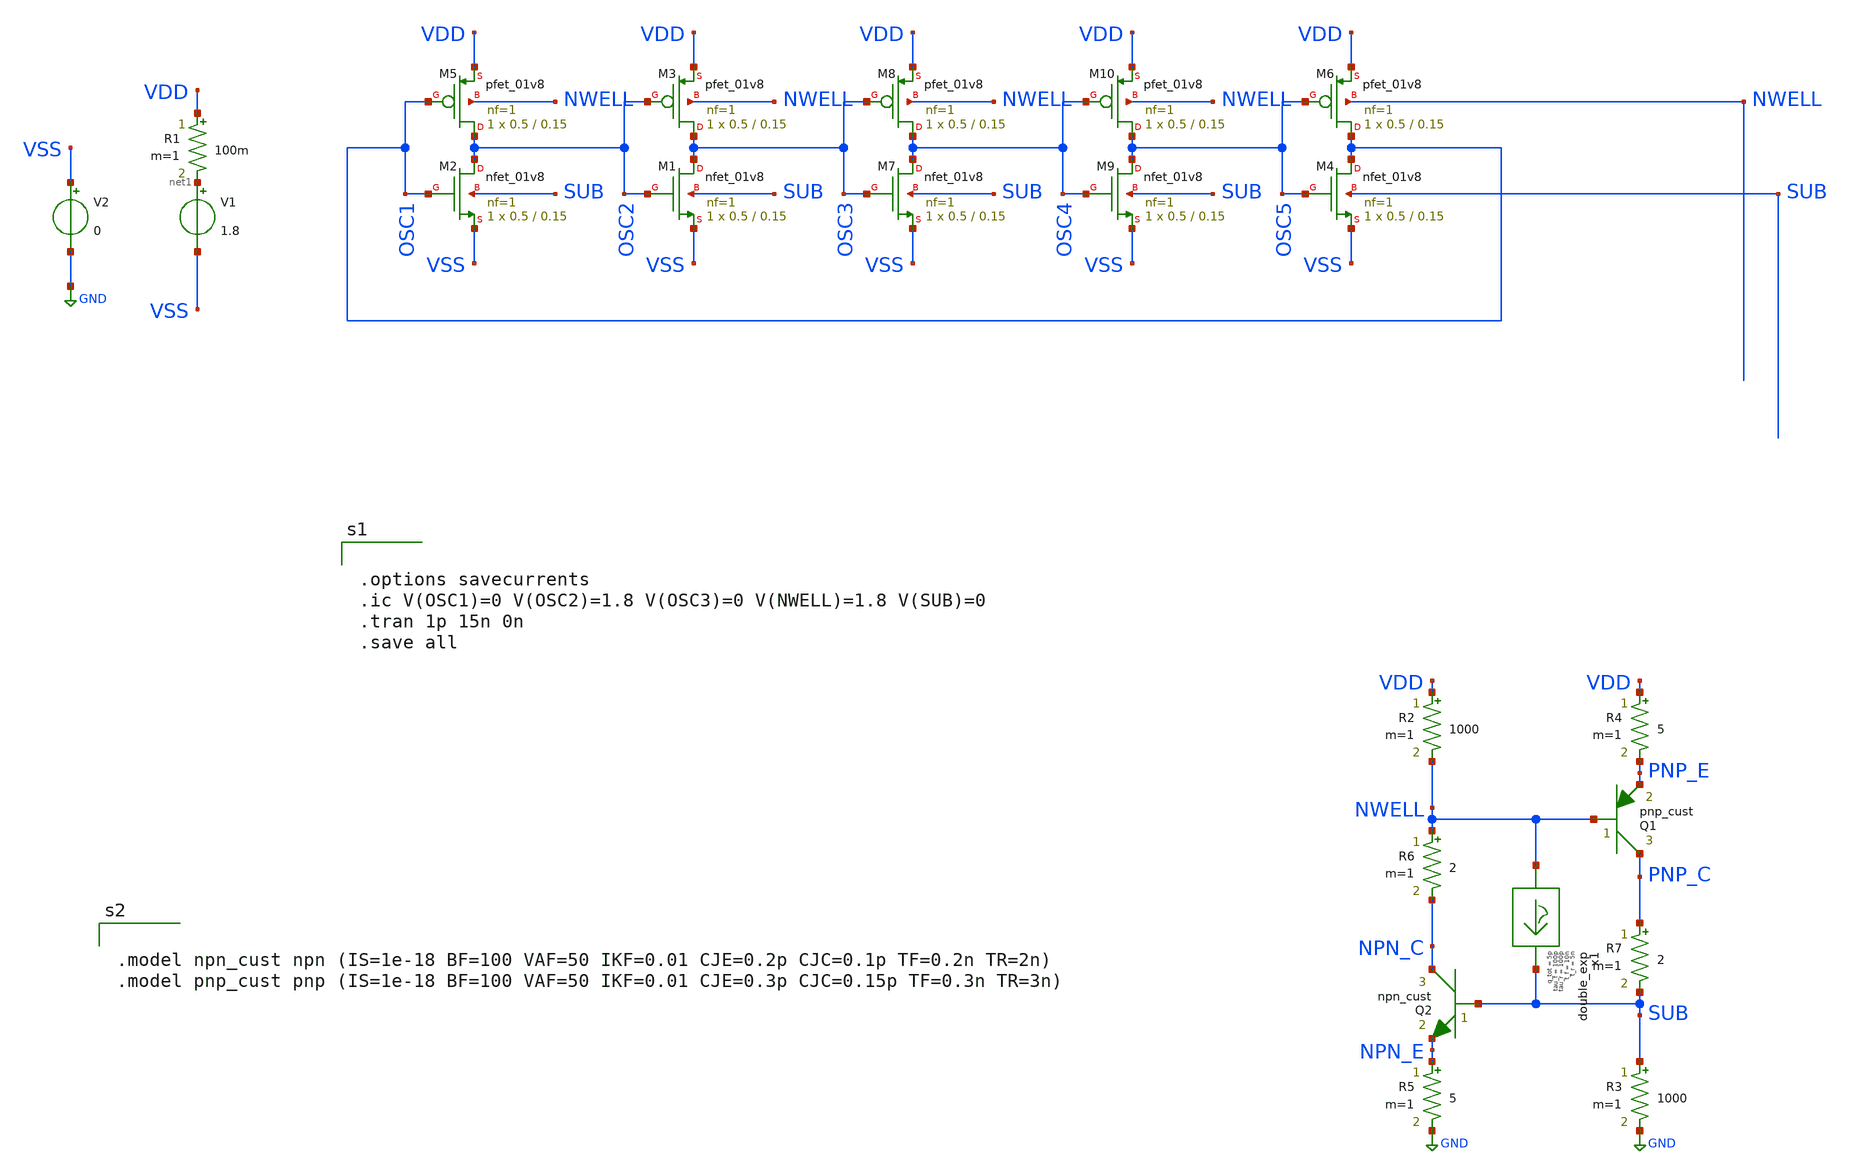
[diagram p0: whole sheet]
** sch_path: latchup/ring_osc_test_intermed.sch
**.subckt ring_osc_test_intermed
XM2 OSC2 OSC1 VSS SUB sky130_fd_pr__nfet_01v8 L=0.15 W=0.5 nf=1 ad='int((nf+1)/2) * W/nf * 0.29' as='int((nf+2)/2) * W/nf * 0.29'
+ pd='2*int((nf+1)/2) * (W/nf + 0.29)' ps='2*int((nf+2)/2) * (W/nf + 0.29)' nrd='0.29 / W' nrs='0.29 / W'
+ sa=0 sb=0 sd=0 mult=1 m=1
XM5 OSC2 OSC1 VDD NWELL sky130_fd_pr__pfet_01v8 L=0.15 W=0.5 nf=1 ad='int((nf+1)/2) * W/nf * 0.29' as='int((nf+2)/2) * W/nf * 0.29'
+ pd='2*int((nf+1)/2) * (W/nf + 0.29)' ps='2*int((nf+2)/2) * (W/nf + 0.29)' nrd='0.29 / W' nrs='0.29 / W'
+ sa=0 sb=0 sd=0 mult=1 m=1
XM1 OSC3 OSC2 VSS SUB sky130_fd_pr__nfet_01v8 L=0.15 W=0.5 nf=1 ad='int((nf+1)/2) * W/nf * 0.29' as='int((nf+2)/2) * W/nf * 0.29'
+ pd='2*int((nf+1)/2) * (W/nf + 0.29)' ps='2*int((nf+2)/2) * (W/nf + 0.29)' nrd='0.29 / W' nrs='0.29 / W'
+ sa=0 sb=0 sd=0 mult=1 m=1
XM3 OSC3 OSC2 VDD NWELL sky130_fd_pr__pfet_01v8 L=0.15 W=0.5 nf=1 ad='int((nf+1)/2) * W/nf * 0.29' as='int((nf+2)/2) * W/nf * 0.29'
+ pd='2*int((nf+1)/2) * (W/nf + 0.29)' ps='2*int((nf+2)/2) * (W/nf + 0.29)' nrd='0.29 / W' nrs='0.29 / W'
+ sa=0 sb=0 sd=0 mult=1 m=1
XM4 OSC1 OSC5 VSS SUB sky130_fd_pr__nfet_01v8 L=0.15 W=0.5 nf=1 ad='int((nf+1)/2) * W/nf * 0.29' as='int((nf+2)/2) * W/nf * 0.29'
+ pd='2*int((nf+1)/2) * (W/nf + 0.29)' ps='2*int((nf+2)/2) * (W/nf + 0.29)' nrd='0.29 / W' nrs='0.29 / W'
+ sa=0 sb=0 sd=0 mult=1 m=1
XM6 OSC1 OSC5 VDD NWELL sky130_fd_pr__pfet_01v8 L=0.15 W=0.5 nf=1 ad='int((nf+1)/2) * W/nf * 0.29' as='int((nf+2)/2) * W/nf * 0.29'
+ pd='2*int((nf+1)/2) * (W/nf + 0.29)' ps='2*int((nf+2)/2) * (W/nf + 0.29)' nrd='0.29 / W' nrs='0.29 / W'
+ sa=0 sb=0 sd=0 mult=1 m=1
V1 net1 VSS 1.8
V2 VSS GND 0
R1 VDD net1 100m m=1
XM7 OSC4 OSC3 VSS SUB sky130_fd_pr__nfet_01v8 L=0.15 W=0.5 nf=1 ad='int((nf+1)/2) * W/nf * 0.29' as='int((nf+2)/2) * W/nf * 0.29'
+ pd='2*int((nf+1)/2) * (W/nf + 0.29)' ps='2*int((nf+2)/2) * (W/nf + 0.29)' nrd='0.29 / W' nrs='0.29 / W'
+ sa=0 sb=0 sd=0 mult=1 m=1
XM8 OSC4 OSC3 VDD NWELL sky130_fd_pr__pfet_01v8 L=0.15 W=0.5 nf=1 ad='int((nf+1)/2) * W/nf * 0.29' as='int((nf+2)/2) * W/nf * 0.29'
+ pd='2*int((nf+1)/2) * (W/nf + 0.29)' ps='2*int((nf+2)/2) * (W/nf + 0.29)' nrd='0.29 / W' nrs='0.29 / W'
+ sa=0 sb=0 sd=0 mult=1 m=1
XM9 OSC5 OSC4 VSS SUB sky130_fd_pr__nfet_01v8 L=0.15 W=0.5 nf=1 ad='int((nf+1)/2) * W/nf * 0.29' as='int((nf+2)/2) * W/nf * 0.29'
+ pd='2*int((nf+1)/2) * (W/nf + 0.29)' ps='2*int((nf+2)/2) * (W/nf + 0.29)' nrd='0.29 / W' nrs='0.29 / W'
+ sa=0 sb=0 sd=0 mult=1 m=1
XM10 OSC5 OSC4 VDD NWELL sky130_fd_pr__pfet_01v8 L=0.15 W=0.5 nf=1 ad='int((nf+1)/2) * W/nf * 0.29' as='int((nf+2)/2) * W/nf * 0.29'
+ pd='2*int((nf+1)/2) * (W/nf + 0.29)' ps='2*int((nf+2)/2) * (W/nf + 0.29)' nrd='0.29 / W' nrs='0.29 / W'
+ sa=0 sb=0 sd=0 mult=1 m=1
Q1 PNP_C NWELL PNP_E pnp_cust area=1 m=1
Q2 NPN_C SUB NPN_E npn_cust area=1 m=1
R3 SUB GND 1000 m=1
R4 VDD PNP_E 5 m=1
R2 VDD NWELL 1000 m=1
R5 NPN_E GND 5 m=1
R6 NWELL NPN_C 2 m=1
R7 PNP_C SUB 2 m=1
x1 NWELL SUB double_exp t_r=5n tau_r=100p t_f=10n tau_f=100p q_tot=5p
**** begin user architecture code


.options savecurrents
.ic V(OSC1)=0 V(OSC2)=1.8 V(OSC3)=0 V(NWELL)=1.8 V(SUB)=0
.tran 1p 15n 0n
.save all



** opencircuitdesign pdks install
.lib $::SKYWATER_MODELS/sky130.lib.spice tt




.include /usr/local/share/rad_modeling_blocks/rad_modeling_blocks.spice




.model npn_cust npn (IS=1e-18 BF=100 VAF=50 IKF=0.01 CJE=0.2p CJC=0.1p TF=0.2n TR=2n)
.model pnp_cust pnp (IS=1e-18 BF=100 VAF=50 IKF=0.01 CJE=0.3p CJC=0.15p TF=0.3n TR=3n)


**** end user architecture code
**.ends

* expanding   symbol:  double_exp.sym # of pins=2
** sym_path: xschem_rad_library/double_exp.sym
** sch_path: xschem_rad_library/double_exp.sch
.subckt double_exp in out  t_r=0 t_f=0 tau_r=0 tau_f=0 q_tot=0
*.opin OUT
*.ipin IN
I1 IN OUT EXP(0 {q_tot / (t_f-t_r+tau_f-tau_r)} {t_r} {tau_r} {t_f} {tau_f})
.ends

.GLOBAL GND
.end
